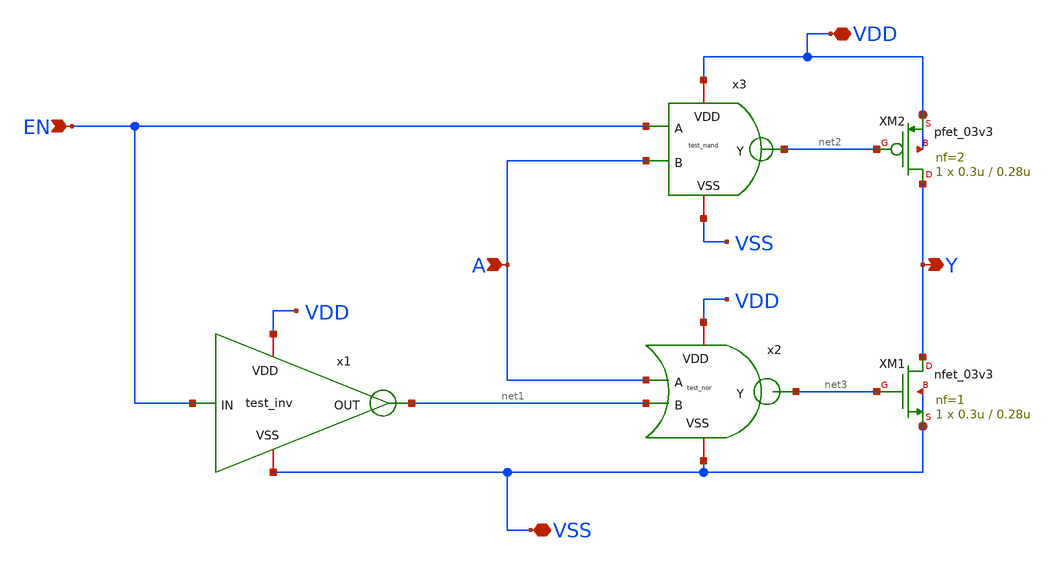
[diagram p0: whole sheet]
** sch_path: designs/libs/core_test/test_tristate/test_tristate.sch
**.subckt test_tristate EN A VDD VSS Y
*.ipin EN
*.ipin A
*.iopin VDD
*.iopin VSS
*.opin Y
x1 VDD net1 EN VSS test_inv
x2 VDD A net1 net3 VSS test_nor
x3 VDD EN net2 A VSS test_nand
XM1 Y net3 VSS VSS nfet_03v3 L=0.28u W=0.3u nf=1 ad='int((nf+1)/2) * W/nf * 0.18u' as='int((nf+2)/2) * W/nf * 0.18u'
+ pd='2*int((nf+1)/2) * (W/nf + 0.18u)' ps='2*int((nf+2)/2) * (W/nf + 0.18u)' nrd='0.18u / W' nrs='0.18u / W'
+ sa=0 sb=0 sd=0 m=1
XM2 Y net2 VDD VDD pfet_03v3 L=0.28u W=0.3u nf=2 ad='int((nf+1)/2) * W/nf * 0.18u' as='int((nf+2)/2) * W/nf * 0.18u'
+ pd='2*int((nf+1)/2) * (W/nf + 0.18u)' ps='2*int((nf+2)/2) * (W/nf + 0.18u)' nrd='0.18u / W' nrs='0.18u / W'
+ sa=0 sb=0 sd=0 m=1
**.ends
.end
